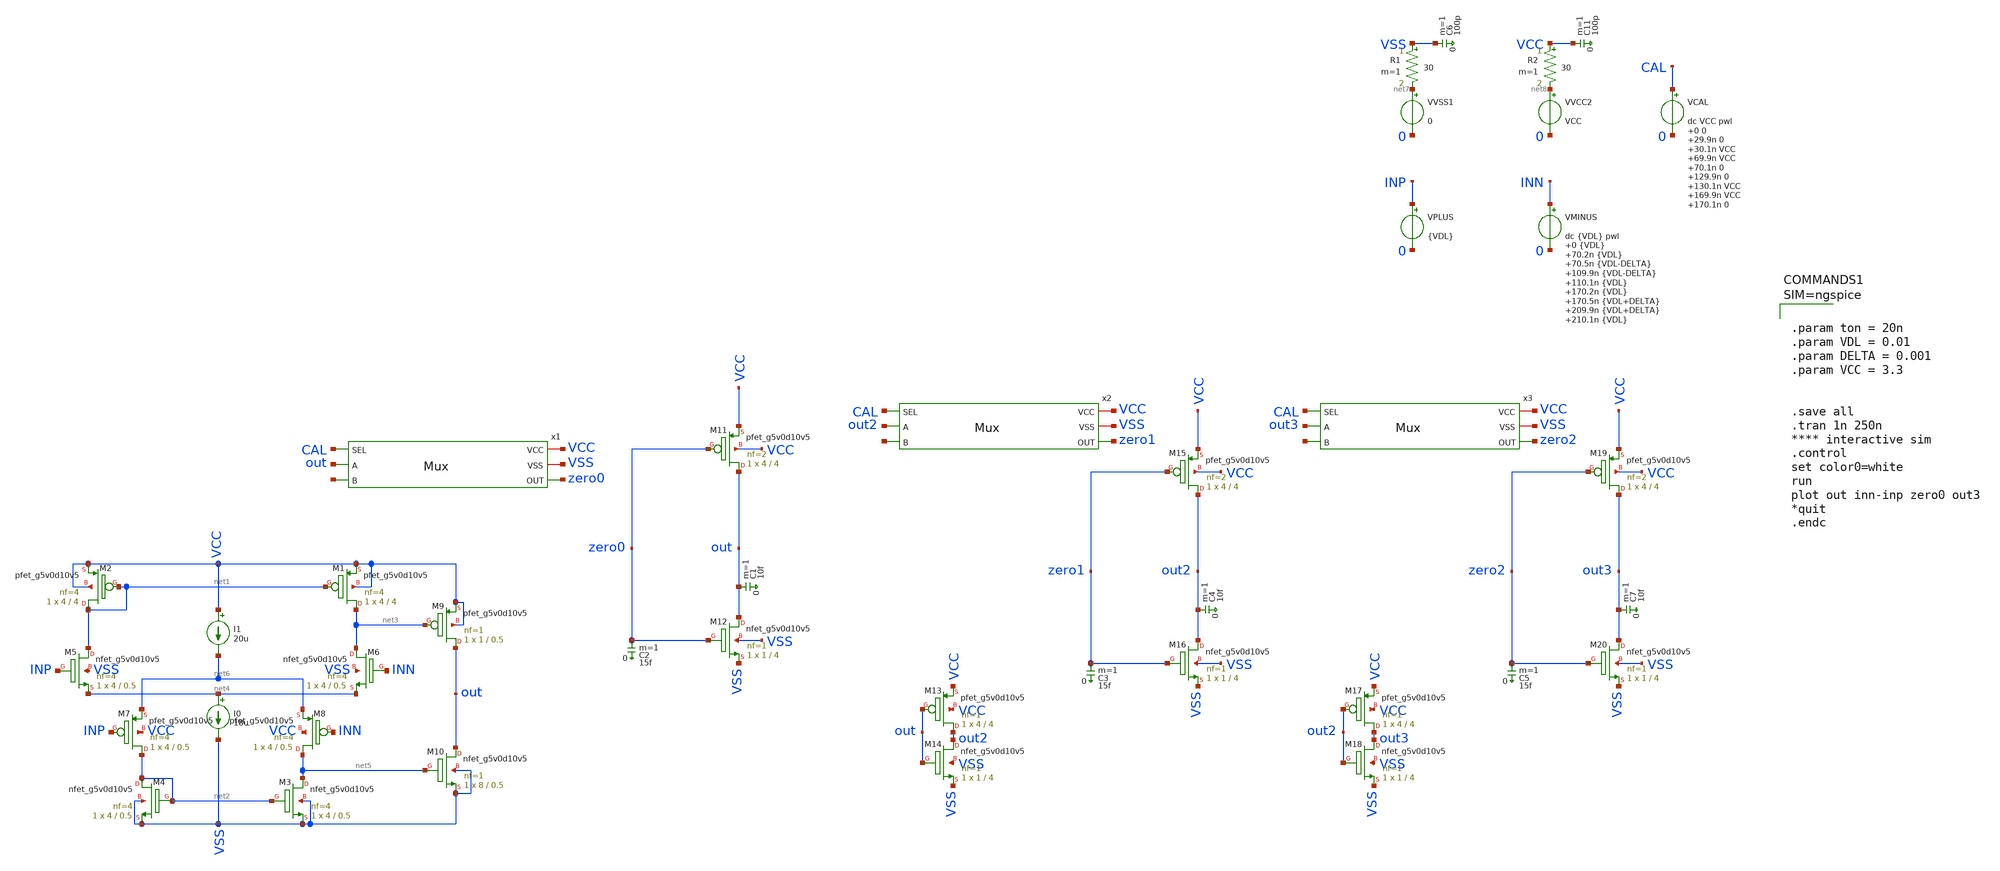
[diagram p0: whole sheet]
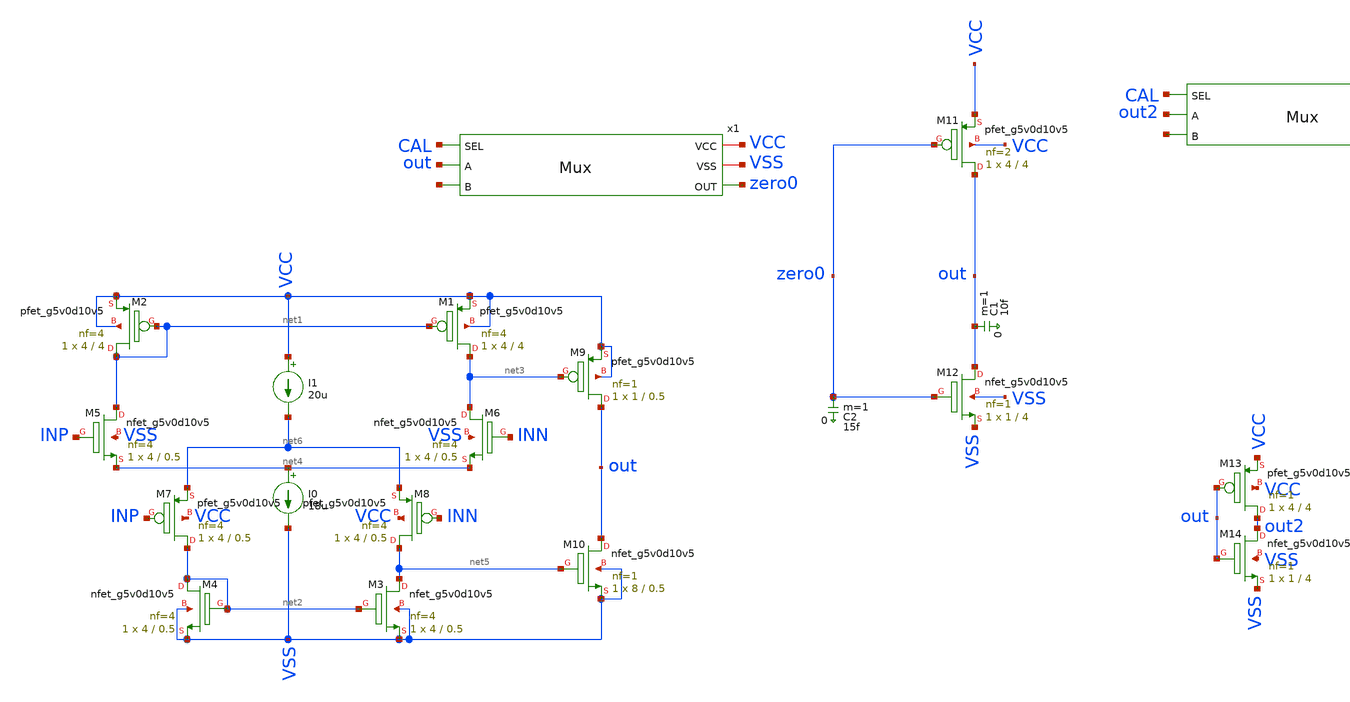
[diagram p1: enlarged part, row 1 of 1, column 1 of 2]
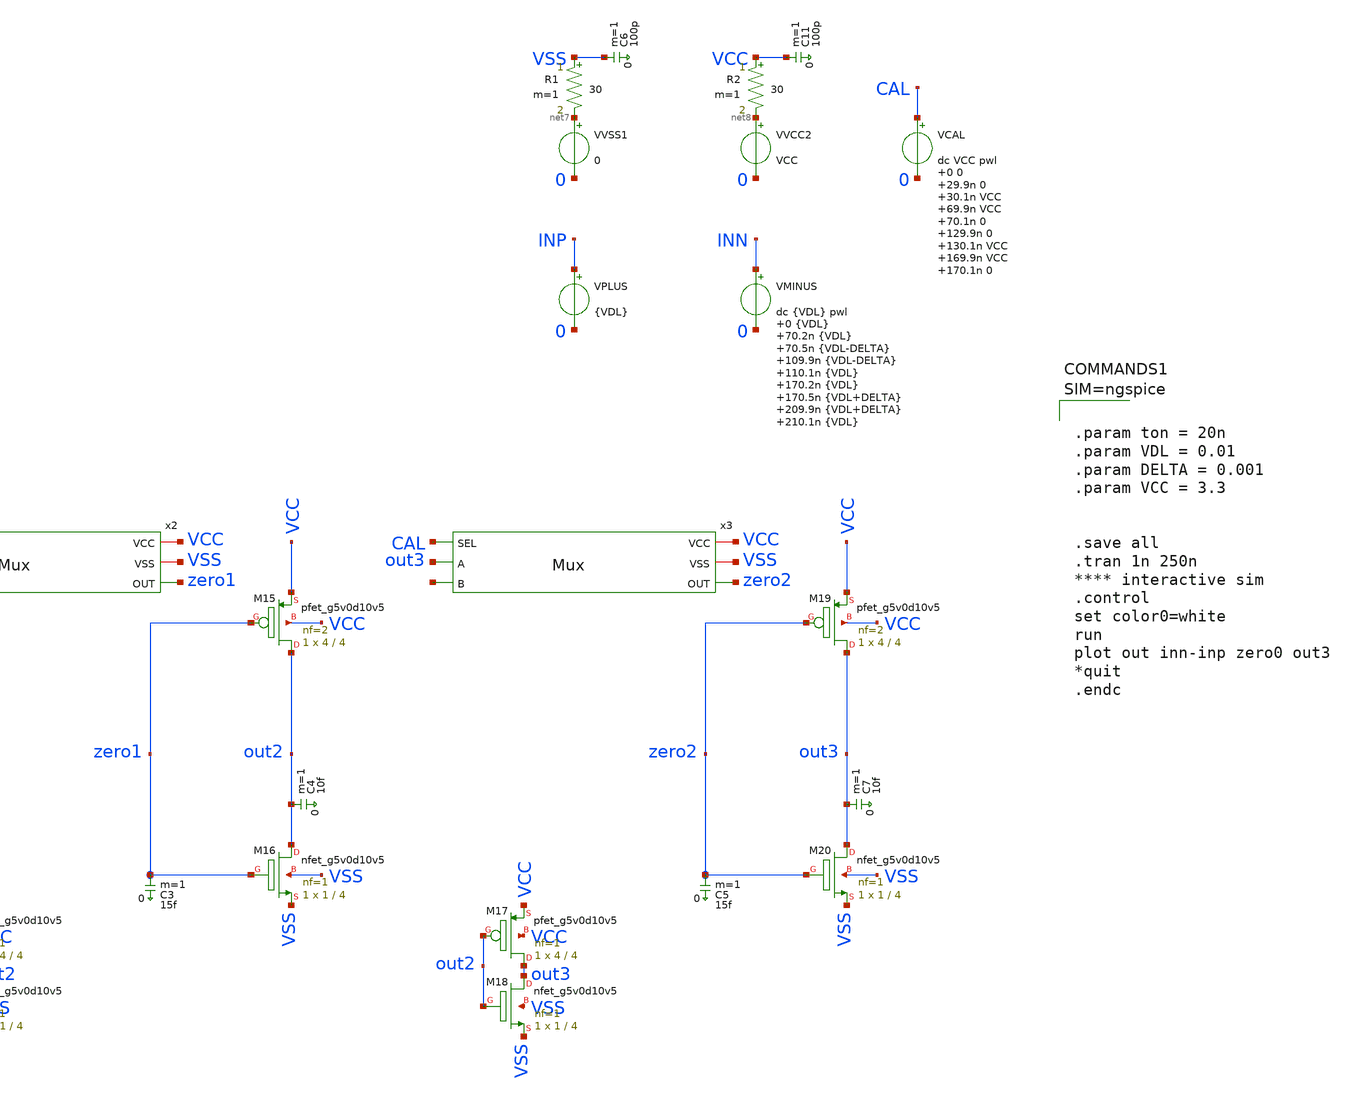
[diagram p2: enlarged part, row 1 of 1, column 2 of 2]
** sch_path: Comparator/schematic/self_calibrating/self_calibrating.sch
.lib $::SKYWATER_MODELS/sky130.lib.spice.tt.red tt
.include $::SKYWATER_STDCELLS/sky130_fd_sc_hd.spice

**.subckt self_calibrating
XM1 net3 net1 VCC VCC sky130_fd_pr__pfet_g5v0d10v5 L=4 W=4 nf=4 ad='int((nf+1)/2) * W/nf * 0.29' as='int((nf+2)/2) * W/nf * 0.29'
+ pd='2*int((nf+1)/2) * (W/nf + 0.29)' ps='2*int((nf+2)/2) * (W/nf + 0.29)' nrd='0.29 / W' nrs='0.29 / W'
+ sa=0 sb=0 sd=0 mult=1 m=1
XM2 net1 net1 VCC VCC sky130_fd_pr__pfet_g5v0d10v5 L=4 W=4 nf=4 ad='int((nf+1)/2) * W/nf * 0.29' as='int((nf+2)/2) * W/nf * 0.29'
+ pd='2*int((nf+1)/2) * (W/nf + 0.29)' ps='2*int((nf+2)/2) * (W/nf + 0.29)' nrd='0.29 / W' nrs='0.29 / W'
+ sa=0 sb=0 sd=0 mult=1 m=1
XM3 net5 net2 VSS VSS sky130_fd_pr__nfet_g5v0d10v5 L=0.5 W=4 nf=4 ad='int((nf+1)/2) * W/nf * 0.29' as='int((nf+2)/2) * W/nf * 0.29'
+ pd='2*int((nf+1)/2) * (W/nf + 0.29)' ps='2*int((nf+2)/2) * (W/nf + 0.29)' nrd='0.29 / W' nrs='0.29 / W'
+ sa=0 sb=0 sd=0 mult=1 m=1
XM4 net2 net2 VSS VSS sky130_fd_pr__nfet_g5v0d10v5 L=0.5 W=4 nf=4 ad='int((nf+1)/2) * W/nf * 0.29' as='int((nf+2)/2) * W/nf * 0.29'
+ pd='2*int((nf+1)/2) * (W/nf + 0.29)' ps='2*int((nf+2)/2) * (W/nf + 0.29)' nrd='0.29 / W' nrs='0.29 / W'
+ sa=0 sb=0 sd=0 mult=1 m=1
XM5 net1 INP net4 VSS sky130_fd_pr__nfet_g5v0d10v5 L=0.5 W=4 nf=4 ad='int((nf+1)/2) * W/nf * 0.29' as='int((nf+2)/2) * W/nf * 0.29'
+ pd='2*int((nf+1)/2) * (W/nf + 0.29)' ps='2*int((nf+2)/2) * (W/nf + 0.29)' nrd='0.29 / W' nrs='0.29 / W'
+ sa=0 sb=0 sd=0 mult=1 m=1
XM6 net3 INN net4 VSS sky130_fd_pr__nfet_g5v0d10v5 L=0.5 W=4 nf=4 ad='int((nf+1)/2) * W/nf * 0.29' as='int((nf+2)/2) * W/nf * 0.29'
+ pd='2*int((nf+1)/2) * (W/nf + 0.29)' ps='2*int((nf+2)/2) * (W/nf + 0.29)' nrd='0.29 / W' nrs='0.29 / W'
+ sa=0 sb=0 sd=0 mult=1 m=1
I0 net4 VSS 18u
XM7 net2 INP net6 VCC sky130_fd_pr__pfet_g5v0d10v5 L=0.5 W=4 nf=4 ad='int((nf+1)/2) * W/nf * 0.29' as='int((nf+2)/2) * W/nf * 0.29'
+ pd='2*int((nf+1)/2) * (W/nf + 0.29)' ps='2*int((nf+2)/2) * (W/nf + 0.29)' nrd='0.29 / W' nrs='0.29 / W'
+ sa=0 sb=0 sd=0 mult=1 m=1
XM8 net5 INN net6 VCC sky130_fd_pr__pfet_g5v0d10v5 L=0.5 W=4 nf=4 ad='int((nf+1)/2) * W/nf * 0.29' as='int((nf+2)/2) * W/nf * 0.29'
+ pd='2*int((nf+1)/2) * (W/nf + 0.29)' ps='2*int((nf+2)/2) * (W/nf + 0.29)' nrd='0.29 / W' nrs='0.29 / W'
+ sa=0 sb=0 sd=0 mult=1 m=1
I1 VCC net6 20u
XM9 out net3 VCC VCC sky130_fd_pr__pfet_g5v0d10v5 L=0.5 W=1 nf=1 ad='int((nf+1)/2) * W/nf * 0.29' as='int((nf+2)/2) * W/nf * 0.29'
+ pd='2*int((nf+1)/2) * (W/nf + 0.29)' ps='2*int((nf+2)/2) * (W/nf + 0.29)' nrd='0.29 / W' nrs='0.29 / W'
+ sa=0 sb=0 sd=0 mult=1 m=1
XM10 out net5 VSS VSS sky130_fd_pr__nfet_g5v0d10v5 L=0.5 W=8 nf=1 ad='int((nf+1)/2) * W/nf * 0.29' as='int((nf+2)/2) * W/nf * 0.29'
+ pd='2*int((nf+1)/2) * (W/nf + 0.29)' ps='2*int((nf+2)/2) * (W/nf + 0.29)' nrd='0.29 / W' nrs='0.29 / W'
+ sa=0 sb=0 sd=0 mult=1 m=1
XM11 out zero0 VCC VCC sky130_fd_pr__pfet_g5v0d10v5 L=4 W=4 nf=2 ad='int((nf+1)/2) * W/nf * 0.29' as='int((nf+2)/2) * W/nf * 0.29'
+ pd='2*int((nf+1)/2) * (W/nf + 0.29)' ps='2*int((nf+2)/2) * (W/nf + 0.29)' nrd='0.29 / W' nrs='0.29 / W'
+ sa=0 sb=0 sd=0 mult=1 m=1
VVSS1 net7 0 0
R1 VSS net7 30 m=1
C6 VSS 0 100p m=1
VVCC2 net8 0 VCC
R2 VCC net8 30 m=1
C11 VCC 0 100p m=1
VPLUS INP 0 {VDL}
VMINUS INN 0 dc {VDL} pwl 0 {VDL} 70.2n {VDL} 70.5n {VDL-DELTA} 109.9n {VDL-DELTA} 110.1n {VDL} 170.2n
+ {VDL} 170.5n {VDL+DELTA} 209.9n {VDL+DELTA} 210.1n {VDL}
VCAL CAL 0 dc VCC pwl 0 0 29.9n 0 30.1n VCC 69.9n VCC 70.1n 0 129.9n 0 130.1n VCC 169.9n VCC 170.1n
+ 0
C2 zero0 0 15f m=1
XM12 out zero0 VSS VSS sky130_fd_pr__nfet_g5v0d10v5 L=4 W=1 nf=1 ad='int((nf+1)/2) * W/nf * 0.29' as='int((nf+2)/2) * W/nf * 0.29'
+ pd='2*int((nf+1)/2) * (W/nf + 0.29)' ps='2*int((nf+2)/2) * (W/nf + 0.29)' nrd='0.29 / W' nrs='0.29 / W'
+ sa=0 sb=0 sd=0 mult=1 m=1
x1 VCC VSS CAL zero0 out net9 Mux
C1 out 0 10f m=1
XM13 out2 out VCC VCC sky130_fd_pr__pfet_g5v0d10v5 L=4 W=4 nf=1 ad='int((nf+1)/2) * W/nf * 0.29' as='int((nf+2)/2) * W/nf * 0.29'
+ pd='2*int((nf+1)/2) * (W/nf + 0.29)' ps='2*int((nf+2)/2) * (W/nf + 0.29)' nrd='0.29 / W' nrs='0.29 / W'
+ sa=0 sb=0 sd=0 mult=1 m=1
XM14 out2 out VSS VSS sky130_fd_pr__nfet_g5v0d10v5 L=4 W=1 nf=1 ad='int((nf+1)/2) * W/nf * 0.29' as='int((nf+2)/2) * W/nf * 0.29'
+ pd='2*int((nf+1)/2) * (W/nf + 0.29)' ps='2*int((nf+2)/2) * (W/nf + 0.29)' nrd='0.29 / W' nrs='0.29 / W'
+ sa=0 sb=0 sd=0 mult=1 m=1
x2 VCC VSS CAL zero1 out2 net10 Mux
XM15 out2 zero1 VCC VCC sky130_fd_pr__pfet_g5v0d10v5 L=4 W=4 nf=2 ad='int((nf+1)/2) * W/nf * 0.29' as='int((nf+2)/2) * W/nf * 0.29'
+ pd='2*int((nf+1)/2) * (W/nf + 0.29)' ps='2*int((nf+2)/2) * (W/nf + 0.29)' nrd='0.29 / W' nrs='0.29 / W'
+ sa=0 sb=0 sd=0 mult=1 m=1
C3 zero1 0 15f m=1
XM16 out2 zero1 VSS VSS sky130_fd_pr__nfet_g5v0d10v5 L=4 W=1 nf=1 ad='int((nf+1)/2) * W/nf * 0.29' as='int((nf+2)/2) * W/nf * 0.29'
+ pd='2*int((nf+1)/2) * (W/nf + 0.29)' ps='2*int((nf+2)/2) * (W/nf + 0.29)' nrd='0.29 / W' nrs='0.29 / W'
+ sa=0 sb=0 sd=0 mult=1 m=1
C4 out2 0 10f m=1
XM17 out3 out2 VCC VCC sky130_fd_pr__pfet_g5v0d10v5 L=4 W=4 nf=1 ad='int((nf+1)/2) * W/nf * 0.29' as='int((nf+2)/2) * W/nf * 0.29'
+ pd='2*int((nf+1)/2) * (W/nf + 0.29)' ps='2*int((nf+2)/2) * (W/nf + 0.29)' nrd='0.29 / W' nrs='0.29 / W'
+ sa=0 sb=0 sd=0 mult=1 m=1
XM18 out3 out2 VSS VSS sky130_fd_pr__nfet_g5v0d10v5 L=4 W=1 nf=1 ad='int((nf+1)/2) * W/nf * 0.29' as='int((nf+2)/2) * W/nf * 0.29'
+ pd='2*int((nf+1)/2) * (W/nf + 0.29)' ps='2*int((nf+2)/2) * (W/nf + 0.29)' nrd='0.29 / W' nrs='0.29 / W'
+ sa=0 sb=0 sd=0 mult=1 m=1
x3 VCC VSS CAL zero2 out3 net11 Mux
XM19 out3 zero2 VCC VCC sky130_fd_pr__pfet_g5v0d10v5 L=4 W=4 nf=2 ad='int((nf+1)/2) * W/nf * 0.29' as='int((nf+2)/2) * W/nf * 0.29'
+ pd='2*int((nf+1)/2) * (W/nf + 0.29)' ps='2*int((nf+2)/2) * (W/nf + 0.29)' nrd='0.29 / W' nrs='0.29 / W'
+ sa=0 sb=0 sd=0 mult=1 m=1
C5 zero2 0 15f m=1
XM20 out3 zero2 VSS VSS sky130_fd_pr__nfet_g5v0d10v5 L=4 W=1 nf=1 ad='int((nf+1)/2) * W/nf * 0.29' as='int((nf+2)/2) * W/nf * 0.29'
+ pd='2*int((nf+1)/2) * (W/nf + 0.29)' ps='2*int((nf+2)/2) * (W/nf + 0.29)' nrd='0.29 / W' nrs='0.29 / W'
+ sa=0 sb=0 sd=0 mult=1 m=1
C7 out3 0 10f m=1
**** begin user architecture code



.param ton = 20n
.param VDL = 0.01
.param DELTA = 0.001
.param VCC = 3.3


.save all
.tran 1n 250n
**** interactive sim
.control
set color0=white
run
plot out inn-inp zero0 out3
*quit
.endc



**** end user architecture code
**.ends
.end
